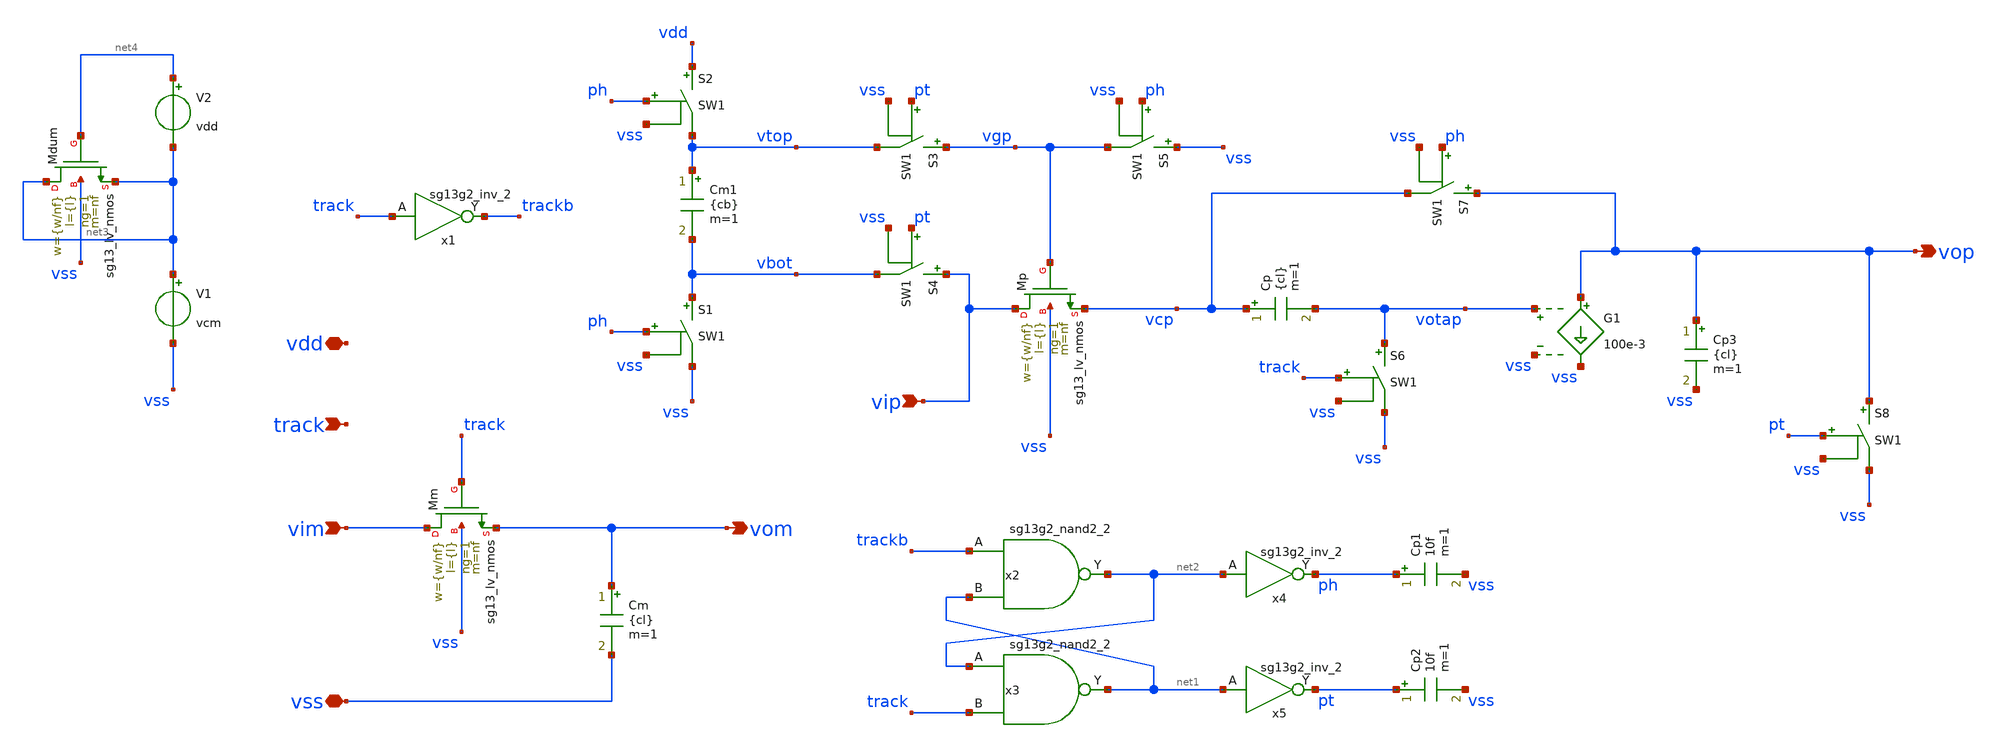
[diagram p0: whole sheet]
** sch_path: th_nmos/xschem/th_boot_ota.sch
* IHP-GmbH/IHP-Open-PDK/ihp-sg13g2/libs.tech/xschem/sg13g2_stdcells/sg13g2_inv_2.sch:
* Copyright 2023 IHP PDK Authors
* Licensed under the Apache License, Version 2.0 (the "License");
**.subckt th_boot_ota vip vim vom track vss vdd vop
*.ipin vip
*.ipin vim
*.opin vom
*.ipin track
*.iopin vss
*.iopin vdd
*.opin vop
XMp vip vgp vcp vss sg13_lv_nmos w={w/nf} l={l} ng=1 m=nf mm_ok=1
XMm vim track vom vss sg13_lv_nmos w={w/nf} l={l} ng=1 m=nf mm_ok=1
Cm vom vss {cl} m=1
Cm1 vtop vbot {cb} m=1
S1 vbot vss ph vss SW1
S2 vdd vtop ph vss SW1
S3 vgp vtop pt vss SW1
S4 vip vbot pt vss SW1
x1 trackb track VDD VSS sg13g2_inv_2
S5 vss vgp ph vss SW1
x2 net2 trackb net1 VDD VSS sg13g2_nand2_2
x3 net1 net2 track VDD VSS sg13g2_nand2_2
x4 ph net2 VDD VSS sg13g2_inv_2
x5 pt net1 VDD VSS sg13g2_inv_2
XMdum net3 net4 net3 vss sg13_lv_nmos w={w/nf} l={l} ng=1 m=nf mm_ok=1
V1 net3 vss vcm
V2 net4 net3 vdd
Cp1 ph vss 10f m=1
Cp2 pt vss 10f m=1
Cp vcp votap {cl} m=1
S6 votap vss track vss SW1
G1 vop vss votap vss 100e-3
S7 vop vcp ph vss SW1
Cp3 vop vss {cl} m=1
S8 vop vss pt vss SW1
**.ends

* expanding   symbol:  sg13g2_stdcells/sg13g2_inv_2.sym # of pins=2
** sym_path: sg13g2_stdcells/sg13g2_inv_2.sym
** sch_path: sg13g2_stdcells/sg13g2_inv_2.sch
.subckt sg13g2_inv_2 Y A VDD VSS
*.opin Y
*.ipin A
*.iopin VDD
*.iopin VSS
XM1 Y A VSS VSS sg13_lv_nmos w=1.48u l=130.00n ng=2 m=1 mm_ok=1
XM2 Y A VDD VDD sg13_lv_pmos w=2.24u l=130.00n ng=2 m=1 mm_ok=1
.ends


* expanding   symbol:  sg13g2_stdcells/sg13g2_nand2_2.sym # of pins=3
** sym_path: sg13g2_stdcells/sg13g2_nand2_2.sym
** sch_path: sg13g2_stdcells/sg13g2_nand2_2.sch
.subckt sg13g2_nand2_2 Y A B VDD VSS
*.iopin VDD
*.iopin VSS
*.opin Y
*.ipin B
*.ipin A
XM1 Y A net1 VSS sg13_lv_nmos w=1.44u l=130.00n ng=2 m=1 mm_ok=1
XM2 net1 B VSS VSS sg13_lv_nmos w=1.44u l=130.00n ng=2 m=1 mm_ok=1
XM3 Y A VDD VDD sg13_lv_pmos w=2.24u l=130.00n ng=2 m=1 mm_ok=1
XM4 Y B VDD VDD sg13_lv_pmos w=2.24u l=130.00n ng=2 m=1 mm_ok=1
.ends

**** begin user architecture code
.MODEL SW1 SW   VT=0.6 VH=0.1  RON=1 ROFF=10G
**** end user architecture code
.end
